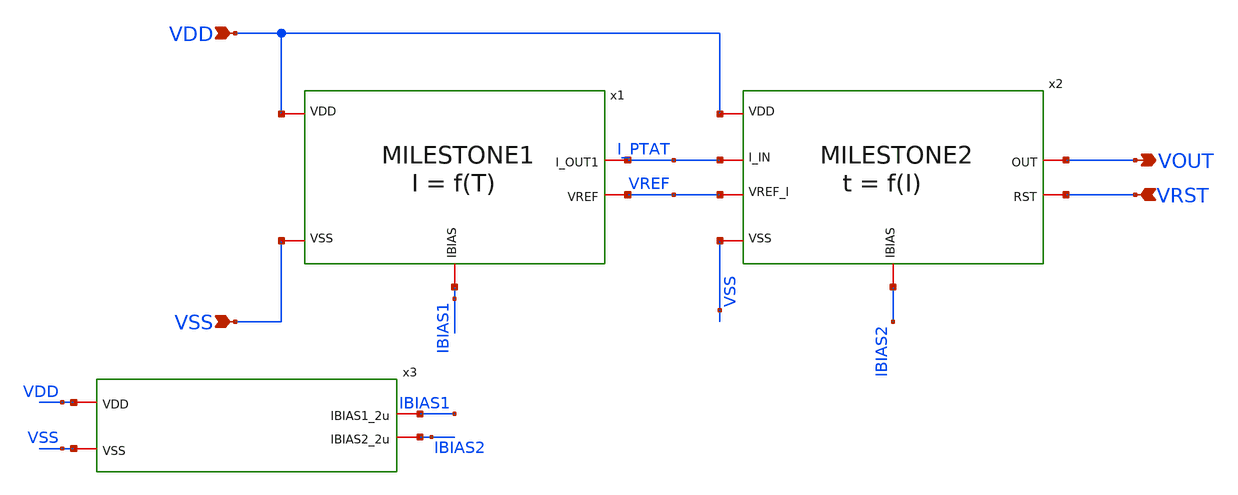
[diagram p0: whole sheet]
** sch_path: design/CNR_GR03_SKY130NM/TOPLEVEL.sch
**.subckt TOPLEVEL VDD VSS VOUT VRST
*.ipin VDD
*.ipin VSS
*.opin VOUT
*.ipin VRST
x1 VDD I_PTAT VREF VSS IBIAS1 MILESTONE1
x2 I_PTAT VREF VOUT VDD VRST VSS IBIAS2 MILESTONE2
x3 VDD IBIAS1 IBIAS2 VSS BIAS
**.ends
.end
